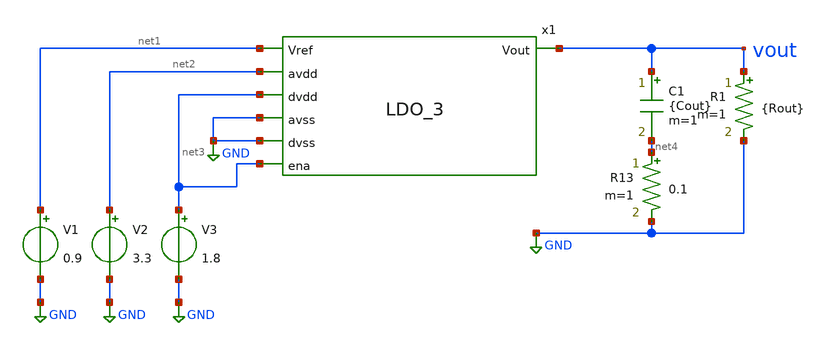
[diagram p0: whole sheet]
** sch_path: cace/test_temp.sch
**.subckt test_temp
V1 net1 GND 0.9
V2 net2 GND 3.3
V3 net3 GND 1.8
C1 vout net4 {Cout} m=1
R13 net4 GND 0.1 m=1
R1 vout GND {Rout} m=1
x1 net1 net2 net3 GND vout GND net3 LDO_3
**** begin user architecture code



.lib /home/dcdc/xschem-src/open_pdks/sky130/sky130A/libs.tech/ngspice/sky130.lib.spice tt

.param Cout = 2.2u
.param Rout = 22.5k
.save all
.option savecurrents

.param TEMGAUSS = agauss(-40, 85, 1)
.option temp = 'TEMGAUSS'

.control
	option seed = 9
	let run = 0
	dowhile run <=100
		save  all
		tran 100u 100000u uic
		remzerovec
		write LDO_v1_temp.raw
		set appendwrite
		reset
		let run = run + 20
		plot V(vout)
	end




.endc

.saveall



**** end user architecture code
**.ends

* expanding   symbol:
*+  /home/dcdc/xschem-src/Work1/chipalooza2024/sky130_deser_ip_lowpowerLDO/xschem/LDO_3.sym # of pins=7
** sym_path: xschem/LDO_3.sym
** sch_path: xschem/LDO_3.sch
.subckt LDO_3 Vref avdd dvdd avss Vout dvss ena
*.ipin avdd
*.ipin dvss
*.ipin dvdd
*.ipin avss
*.ipin ena
*.ipin Vref
*.opin Vout
XM1 vout Vout_fb1 avdd avdd sky130_fd_pr__pfet_01v8_hvt L=0.3 W=99 nf=1 ad='int((nf+1)/2) * W/nf * 0.29'
+ as='int((nf+2)/2) * W/nf * 0.29' pd='2*int((nf+1)/2) * (W/nf + 0.29)' ps='2*int((nf+2)/2) * (W/nf + 0.29)'
+ nrd='0.29 / W' nrs='0.29 / W' sa=0 sb=0 sd=0 mult=1 m=1
XM21 Vout_fb4 net2 avss avss sky130_fd_pr__nfet_01v8_lvt L=0.15 W=6 nf=1 ad='int((nf+1)/2) * W/nf * 0.29'
+ as='int((nf+2)/2) * W/nf * 0.29' pd='2*int((nf+1)/2) * (W/nf + 0.29)' ps='2*int((nf+2)/2) * (W/nf + 0.29)'
+ nrd='0.29 / W' nrs='0.29 / W' sa=0 sb=0 sd=0 mult=1 m=1
XM22 net2 net2 avss avss sky130_fd_pr__nfet_01v8_lvt L=0.15 W=6 nf=1 ad='int((nf+1)/2) * W/nf * 0.29'
+ as='int((nf+2)/2) * W/nf * 0.29' pd='2*int((nf+1)/2) * (W/nf + 0.29)' ps='2*int((nf+2)/2) * (W/nf + 0.29)'
+ nrd='0.29 / W' nrs='0.29 / W' sa=0 sb=0 sd=0 mult=1 m=1
XM23 net4 Vout_fb4 avss avss sky130_fd_pr__nfet_01v8_lvt L=0.15 W=10 nf=1 ad='int((nf+1)/2) * W/nf * 0.29'
+ as='int((nf+2)/2) * W/nf * 0.29' pd='2*int((nf+1)/2) * (W/nf + 0.29)' ps='2*int((nf+2)/2) * (W/nf + 0.29)'
+ nrd='0.29 / W' nrs='0.29 / W' sa=0 sb=0 sd=0 mult=1 m=1
XM2 net4 net5 avdd avdd sky130_fd_pr__pfet_01v8_lvt L=0.35 W=1 nf=1 ad='int((nf+1)/2) * W/nf * 0.29'
+ as='int((nf+2)/2) * W/nf * 0.29' pd='2*int((nf+1)/2) * (W/nf + 0.29)' ps='2*int((nf+2)/2) * (W/nf + 0.29)'
+ nrd='0.29 / W' nrs='0.29 / W' sa=0 sb=0 sd=0 mult=1 m=1
XM3 net2 Vfed net1 avdd sky130_fd_pr__pfet_01v8_lvt L=0.35 W=20 nf=1 ad='int((nf+1)/2) * W/nf * 0.29'
+ as='int((nf+2)/2) * W/nf * 0.29' pd='2*int((nf+1)/2) * (W/nf + 0.29)' ps='2*int((nf+2)/2) * (W/nf + 0.29)'
+ nrd='0.29 / W' nrs='0.29 / W' sa=0 sb=0 sd=0 mult=1 m=1
XM4 Vout_fb4 Vref net1 avdd sky130_fd_pr__pfet_01v8_lvt L=0.35 W=20 nf=1 ad='int((nf+1)/2) * W/nf * 0.29'
+ as='int((nf+2)/2) * W/nf * 0.29' pd='2*int((nf+1)/2) * (W/nf + 0.29)' ps='2*int((nf+2)/2) * (W/nf + 0.29)'
+ nrd='0.29 / W' nrs='0.29 / W' sa=0 sb=0 sd=0 mult=1 m=1
XM5 net1 net5 avdd avdd sky130_fd_pr__pfet_01v8_lvt L=0.35 W=1 nf=1 ad='int((nf+1)/2) * W/nf * 0.29'
+ as='int((nf+2)/2) * W/nf * 0.29' pd='2*int((nf+1)/2) * (W/nf + 0.29)' ps='2*int((nf+2)/2) * (W/nf + 0.29)'
+ nrd='0.29 / W' nrs='0.29 / W' sa=0 sb=0 sd=0 mult=1 m=1
XM6 net5 net5 avdd avdd sky130_fd_pr__pfet_01v8_lvt L=0.35 W=1 nf=1 ad='int((nf+1)/2) * W/nf * 0.29'
+ as='int((nf+2)/2) * W/nf * 0.29' pd='2*int((nf+1)/2) * (W/nf + 0.29)' ps='2*int((nf+2)/2) * (W/nf + 0.29)'
+ nrd='0.29 / W' nrs='0.29 / W' sa=0 sb=0 sd=0 mult=1 m=1
XM7 Vout_fb1 net4 avss net7 sky130_fd_pr__nfet_01v8_lvt L=0.15 W=1 nf=1 ad='int((nf+1)/2) * W/nf * 0.29'
+ as='int((nf+2)/2) * W/nf * 0.29' pd='2*int((nf+1)/2) * (W/nf + 0.29)' ps='2*int((nf+2)/2) * (W/nf + 0.29)'
+ nrd='0.29 / W' nrs='0.29 / W' sa=0 sb=0 sd=0 mult=1 m=1
XM8 Vout_fb1 net5 avdd net8 sky130_fd_pr__pfet_01v8_lvt L=0.35 W=1 nf=1 ad='int((nf+1)/2) * W/nf * 0.29'
+ as='int((nf+2)/2) * W/nf * 0.29' pd='2*int((nf+1)/2) * (W/nf + 0.29)' ps='2*int((nf+2)/2) * (W/nf + 0.29)'
+ nrd='0.29 / W' nrs='0.29 / W' sa=0 sb=0 sd=0 mult=1 m=1
XR8 avss net5 avdd sky130_fd_pr__res_xhigh_po_5p73 L=5.73*25 mult=1 m=1
XC4 Vout_fb4 net3 sky130_fd_pr__cap_mim_m3_2 W=10 L=30 MF=1 m=1
R9 net3 net4 sky130_fd_pr__res_generic_l1 W=1 L=19 m=1
XC2 net4 net6 sky130_fd_pr__cap_mim_m3_2 W=10 L=30 MF=1 m=1
R7 net6 Vout_fb1 sky130_fd_pr__res_generic_l1 W=1 L=19 m=1
XR10 Vfed vout avdd sky130_fd_pr__res_xhigh_po_5p73 L=5.73*25 mult=1 m=1
XR4 avss Vfed avdd sky130_fd_pr__res_xhigh_po_5p73 L=5.73*25 mult=1 m=1
.ends

.GLOBAL GND
.end
